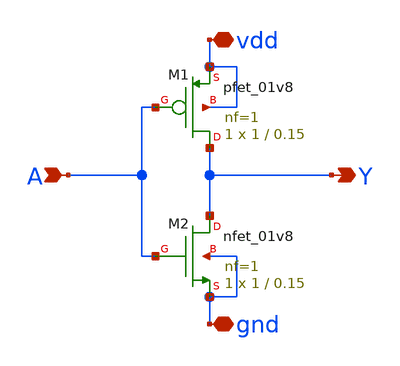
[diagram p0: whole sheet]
** sch_path: inverter130/inverter130_schematic_final.sch
**.subckt inverter130_schematic_final A Y vdd gnd
*.ipin A
*.opin Y
*.iopin vdd
*.iopin gnd
XM1 Y A vdd vdd sky130_fd_pr__pfet_01v8 L=0.15 W=1 nf=1 ad='int((nf+1)/2) * W/nf * 0.29' as='int((nf+2)/2) * W/nf * 0.29'
+ pd='2*int((nf+1)/2) * (W/nf + 0.29)' ps='2*int((nf+2)/2) * (W/nf + 0.29)' nrd='0.29 / W' nrs='0.29 / W'
+ sa=0 sb=0 sd=0 mult=1 m=1
XM2 Y A gnd gnd sky130_fd_pr__nfet_01v8 L=0.15 W=1 nf=1 ad='int((nf+1)/2) * W/nf * 0.29' as='int((nf+2)/2) * W/nf * 0.29'
+ pd='2*int((nf+1)/2) * (W/nf + 0.29)' ps='2*int((nf+2)/2) * (W/nf + 0.29)' nrd='0.29 / W' nrs='0.29 / W'
+ sa=0 sb=0 sd=0 mult=1 m=1
**.ends
.end
